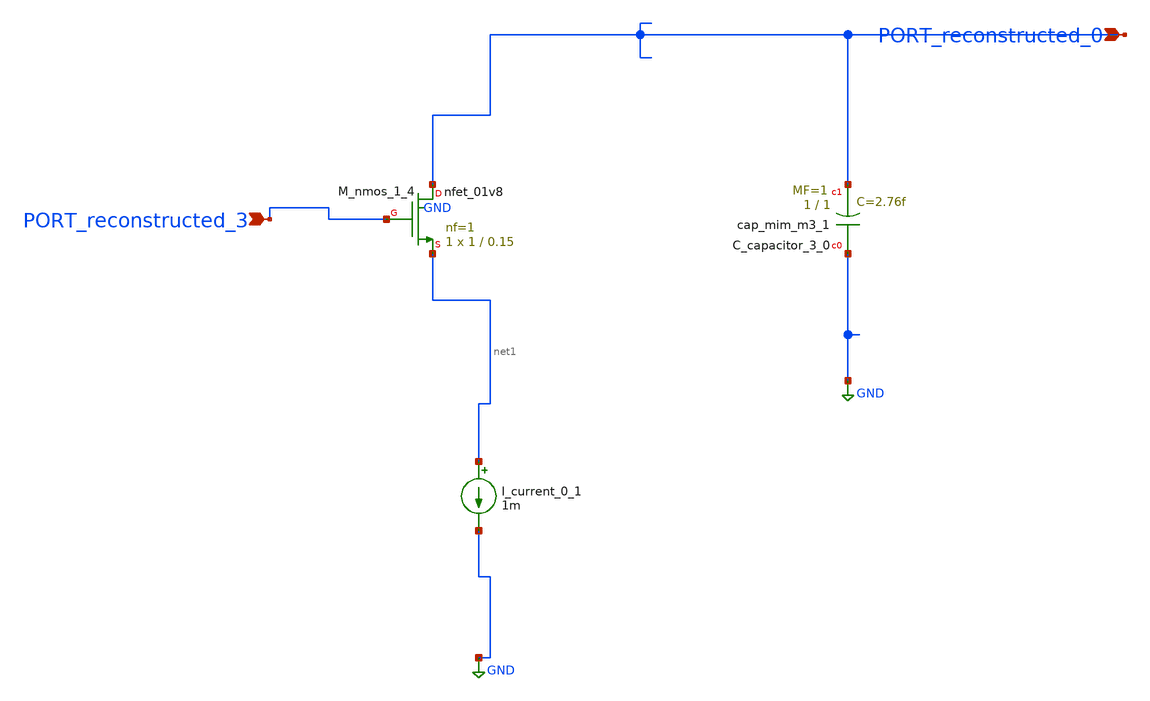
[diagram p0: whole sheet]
** sch_path: schematics/AMSNet/44.sch
**.subckt 44 PORT_reconstructed_3 PORT_reconstructed_0
*.ipin PORT_reconstructed_3
*.ipin PORT_reconstructed_0
XC_capacitor_3_0 GND PORT_reconstructed_0 sky130_fd_pr__cap_mim_m3_1 W=1 L=1 MF=1 m=1
I_current_0_1 net1 GND 1m
XM_nmos_1_4 PORT_reconstructed_0 PORT_reconstructed_3 net1 GND sky130_fd_pr__nfet_01v8 L=0.15 W=1 nf=1
+ ad='int((1 + 1)/2) * 1 / 1 * 0.29' as='int((1 + 2)/2) * 1 / 1 * 0.29' pd='2*int((1 + 1)/2) * (1 / 1 + 0.29)'
+ ps='2*int((1 + 2)/2) * (1 / 1 + 0.29)' nrd='0.29 / 1 ' nrs='0.29 / 1 ' sa=0 sb=0 sd=0 mult=1 m=1
**.ends
.GLOBAL GND
.end
